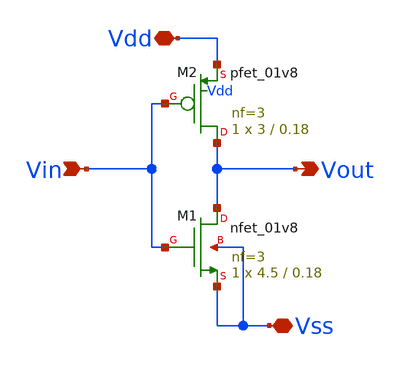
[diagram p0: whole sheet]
** sch_path: Lab1/inverter.sch
**.subckt inverter Vin Vout Vdd Vss
*.ipin Vin
*.opin Vout
*.iopin Vdd
*.iopin Vss
XM1 Vout Vin Vss Vss sky130_fd_pr__nfet_01v8 L=0.18 W=4.5 nf=3 ad='int((3 + 1)/2) * 4.5 / 3 * 0.29' as='int((3 + 2)/2) * 4.5 / 3 * 0.29'
+ pd='2*int((3 + 1)/2) * (4.5 / 3 + 0.29)' ps='2*int((3 + 2)/2) * (4.5 / 3 + 0.29)' nrd='0.29 / 4.5 ' nrs='0.29 / 4.5 '
+ sa=0 sb=0 sd=0 mult=1 m=1
XM2 Vout Vin Vdd Vdd sky130_fd_pr__pfet_01v8 L=0.18 W=3 nf=3 ad='int((3 + 1)/2) * 3 / 3 * 0.29' as='int((3 + 2)/2) * 3 / 3 * 0.29'
+ pd='2*int((3 + 1)/2) * (3 / 3 + 0.29)' ps='2*int((3 + 2)/2) * (3 / 3 + 0.29)' nrd='0.29 / 3 ' nrs='0.29 / 3 '
+ sa=0 sb=0 sd=0 mult=1 m=1
**.ends
.end
